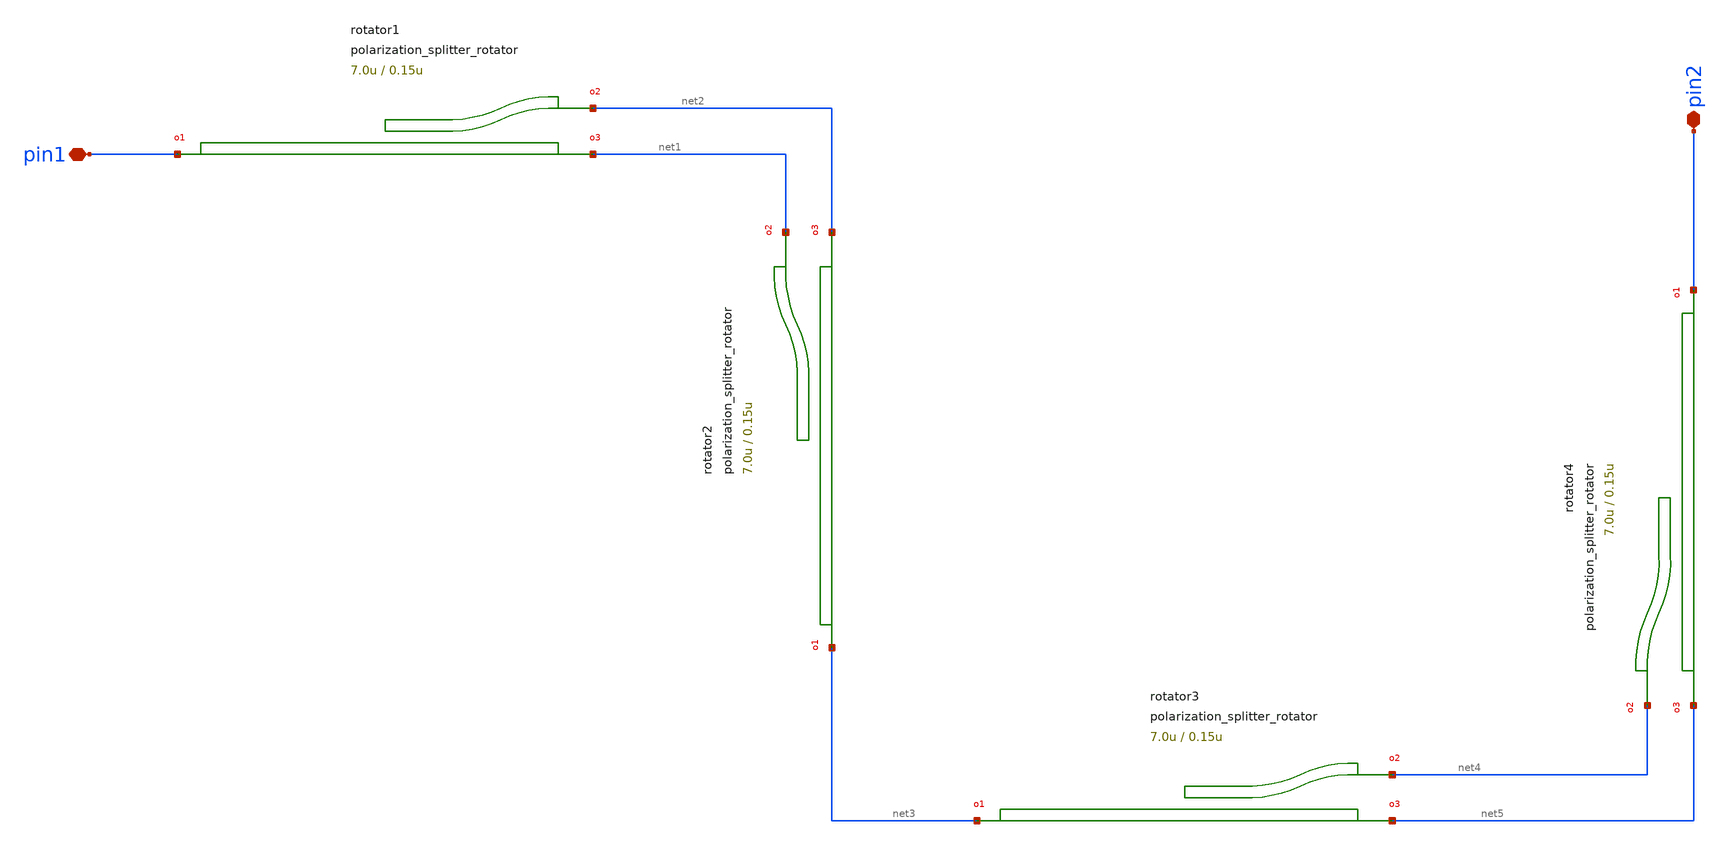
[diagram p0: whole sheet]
** sch_path: xschem/tests/test_sch/test_polarization_splitter_rotator.sch
* Copyright (c) 2024, Mabrains LLC
* Licensed under the GNU Lesser General Public License, Version 3.0 (the "License");
* you may not use this file except in compliance with the License.
* GNU Lesser General Public License
* Version 3, 29 June 2007
* This program is free software: you can redistribute it and/or modify
* it under the terms of the GNU Lesser General Public License as published
* by the Free Software Foundation, either version 3 of the License, or
* (at your option) any later version.
* This program is distributed in the hope that it will be useful,
* but WITHOUT ANY WARRANTY; without even the implied warranty of
* MERCHANTABILITY or FITNESS FOR A PARTICULAR PURPOSE.  See the
* GNU Lesser General Public License for more details.
* You should have received a copy of the GNU Lesser General Public License
* along with this program.  If not, see <https://www.gnu.org/licenses/>.
* SPDX-License-Identifier: LGPL-3.0
**.subckt test_polarization_splitter_rotator pin1 pin2
*.iopin pin1
*.iopin pin2
Protator1 pin1 net2 net1 polarization_splitter_rotator width_taper_in1=0.54u width_taper_in2=0.69u
+ width_taper_in3=0.83u length_taper_in1=4.0u length_taper_in2=44.0u length_taper_in3=44.0u width_coupler_top=0.9u
+ width_coupler_bottom=0.405u length_coupler=7.0u gap=0.15u width_out=0.54u length_out=14.33u dy=5.0u
Protator3 net3 net4 net5 polarization_splitter_rotator width_taper_in1=0.54u width_taper_in2=0.69u
+ width_taper_in3=0.83u length_taper_in1=4.0u length_taper_in2=44.0u length_taper_in3=44.0u width_coupler_top=0.9u
+ width_coupler_bottom=0.405u length_coupler=7.0u gap=0.15u width_out=0.54u length_out=14.33u dy=5.0u
Protator2 net3 net1 net2 polarization_splitter_rotator width_taper_in1=0.54u width_taper_in2=0.69u
+ width_taper_in3=0.83u length_taper_in1=4.0u length_taper_in2=44.0u length_taper_in3=44.0u width_coupler_top=0.9u
+ width_coupler_bottom=0.405u length_coupler=7.0u gap=0.15u width_out=0.54u length_out=14.33u dy=5.0u
Protator4 pin2 net4 net5 polarization_splitter_rotator width_taper_in1=0.54u width_taper_in2=0.69u
+ width_taper_in3=0.83u length_taper_in1=4.0u length_taper_in2=44.0u length_taper_in3=44.0u width_coupler_top=0.9u
+ width_coupler_bottom=0.405u length_coupler=7.0u gap=0.15u width_out=0.54u length_out=14.33u dy=5.0u
**.ends
.end
